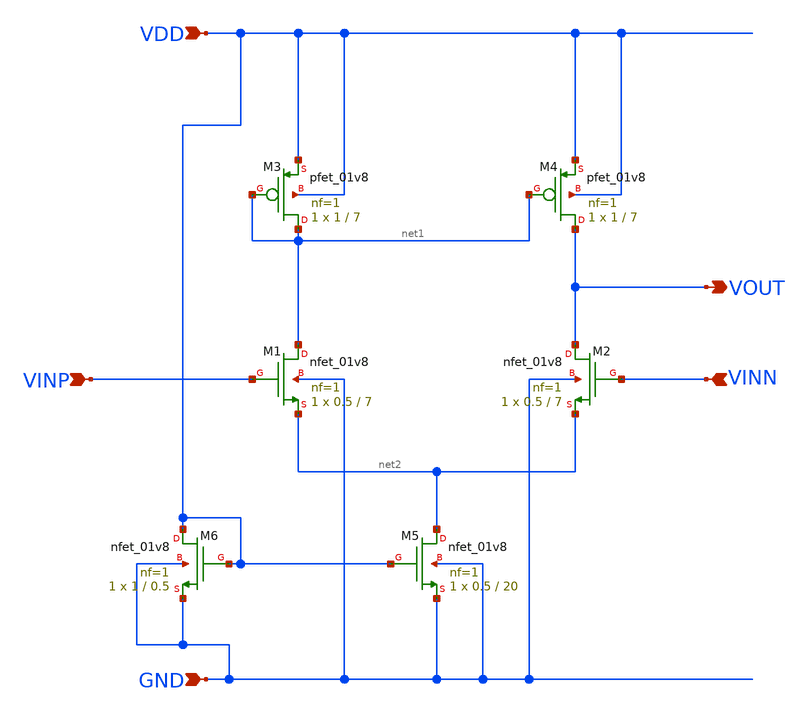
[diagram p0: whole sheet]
** sch_path: xschem/otaq_5t_sky130.sch
**.subckt otaq_5t_sky130 VINP VINN VOUT VDD GND
*.ipin VINP
*.ipin VINN
*.opin VOUT
*.ipin VDD
*.ipin GND
XM5 net2 VDD GND GND sky130_fd_pr__nfet_01v8 L=20 W=0.5 nf=1 ad='int((1 + 1)/2) * 0.5 / 1 * 0.29' as='int((1 + 2)/2) * 0.5 / 1 * 0.29'
+ pd='2*int((1 + 1)/2) * (0.5 / 1 + 0.29)' ps='2*int((1 + 2)/2) * (0.5 / 1 + 0.29)' nrd='0.29 / 0.5 ' nrs='0.29 / 0.5 '
+ sa=0 sb=0 sd=0 mult=1 m=1
XM1 net1 VINP net2 GND sky130_fd_pr__nfet_01v8 L=7 W=0.5 nf=1 ad='int((1 + 1)/2) * 0.5 / 1 * 0.29' as='int((1 + 2)/2) * 0.5 / 1 * 0.29'
+ pd='2*int((1 + 1)/2) * (0.5 / 1 + 0.29)' ps='2*int((1 + 2)/2) * (0.5 / 1 + 0.29)' nrd='0.29 / 0.5 ' nrs='0.29 / 0.5 '
+ sa=0 sb=0 sd=0 mult=1 m=1
XM2 VOUT VINN net2 GND sky130_fd_pr__nfet_01v8 L=7 W=0.5 nf=1 ad='int((1 + 1)/2) * 0.5 / 1 * 0.29' as='int((1 + 2)/2) * 0.5 / 1 * 0.29'
+ pd='2*int((1 + 1)/2) * (0.5 / 1 + 0.29)' ps='2*int((1 + 2)/2) * (0.5 / 1 + 0.29)' nrd='0.29 / 0.5 ' nrs='0.29 / 0.5 '
+ sa=0 sb=0 sd=0 mult=1 m=1
XM3 net1 net1 VDD VDD sky130_fd_pr__pfet_01v8 L=7 W=1 nf=1 ad='int((1 + 1)/2) * 1 / 1 * 0.29' as='int((1 + 2)/2) * 1 / 1 * 0.29'
+ pd='2*int((1 + 1)/2) * (1 / 1 + 0.29)' ps='2*int((1 + 2)/2) * (1 / 1 + 0.29)' nrd='0.29 / 1 ' nrs='0.29 / 1 '
+ sa=0 sb=0 sd=0 mult=1 m=1
XM4 VOUT net1 VDD VDD sky130_fd_pr__pfet_01v8 L=7 W=1 nf=1 ad='int((1 + 1)/2) * 1 / 1 * 0.29' as='int((1 + 2)/2) * 1 / 1 * 0.29'
+ pd='2*int((1 + 1)/2) * (1 / 1 + 0.29)' ps='2*int((1 + 2)/2) * (1 / 1 + 0.29)' nrd='0.29 / 1 ' nrs='0.29 / 1 '
+ sa=0 sb=0 sd=0 mult=1 m=1
XM6 VDD VDD GND GND sky130_fd_pr__nfet_01v8 L=0.5 W=1 nf=1 ad='int((1 + 1)/2) * 1 / 1 * 0.29' as='int((1 + 2)/2) * 1 / 1 * 0.29'
+ pd='2*int((1 + 1)/2) * (1 / 1 + 0.29)' ps='2*int((1 + 2)/2) * (1 / 1 + 0.29)' nrd='0.29 / 1 ' nrs='0.29 / 1 '
+ sa=0 sb=0 sd=0 mult=1 m=1
**.ends
.end
